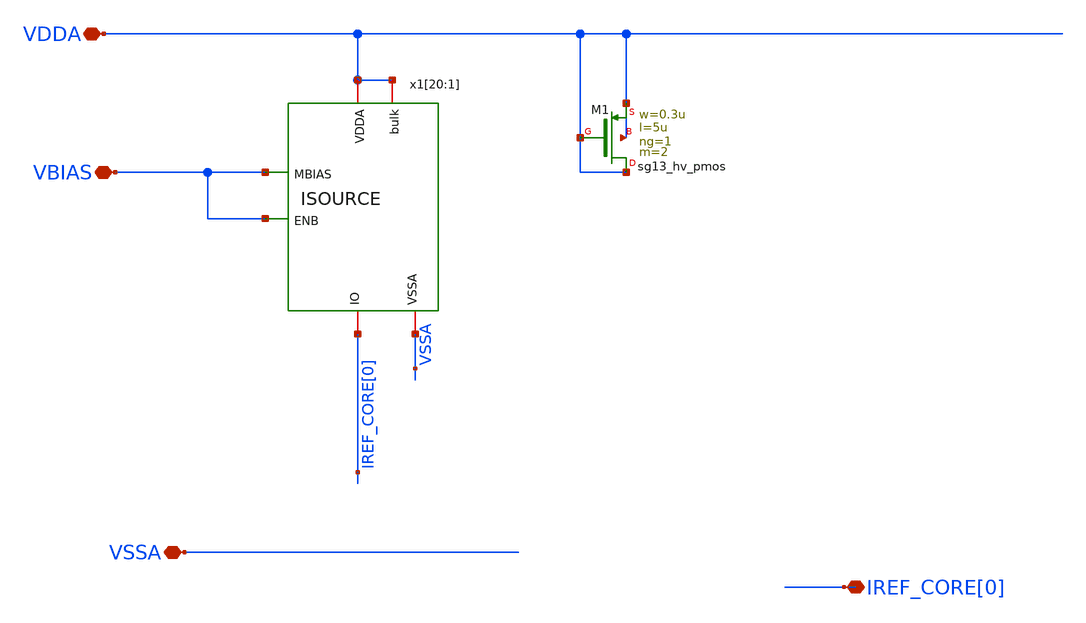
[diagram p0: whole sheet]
** sch_path: DecadeDividerAux.sch
**.subckt DecadeDividerAux VSSA VDDA VBIAS IREF_CORE[0]
*.iopin VSSA
*.iopin VDDA
*.iopin VBIAS
*.iopin IREF_CORE[0]
x1[20] VDDA VBIAS VDDA VBIAS VSSA IREF_CORE[0] ISOURCE
x1[19] VDDA VBIAS VDDA VBIAS VSSA IREF_CORE[0] ISOURCE
x1[18] VDDA VBIAS VDDA VBIAS VSSA IREF_CORE[0] ISOURCE
x1[17] VDDA VBIAS VDDA VBIAS VSSA IREF_CORE[0] ISOURCE
x1[16] VDDA VBIAS VDDA VBIAS VSSA IREF_CORE[0] ISOURCE
x1[15] VDDA VBIAS VDDA VBIAS VSSA IREF_CORE[0] ISOURCE
x1[14] VDDA VBIAS VDDA VBIAS VSSA IREF_CORE[0] ISOURCE
x1[13] VDDA VBIAS VDDA VBIAS VSSA IREF_CORE[0] ISOURCE
x1[12] VDDA VBIAS VDDA VBIAS VSSA IREF_CORE[0] ISOURCE
x1[11] VDDA VBIAS VDDA VBIAS VSSA IREF_CORE[0] ISOURCE
x1[10] VDDA VBIAS VDDA VBIAS VSSA IREF_CORE[0] ISOURCE
x1[9] VDDA VBIAS VDDA VBIAS VSSA IREF_CORE[0] ISOURCE
x1[8] VDDA VBIAS VDDA VBIAS VSSA IREF_CORE[0] ISOURCE
x1[7] VDDA VBIAS VDDA VBIAS VSSA IREF_CORE[0] ISOURCE
x1[6] VDDA VBIAS VDDA VBIAS VSSA IREF_CORE[0] ISOURCE
x1[5] VDDA VBIAS VDDA VBIAS VSSA IREF_CORE[0] ISOURCE
x1[4] VDDA VBIAS VDDA VBIAS VSSA IREF_CORE[0] ISOURCE
x1[3] VDDA VBIAS VDDA VBIAS VSSA IREF_CORE[0] ISOURCE
x1[2] VDDA VBIAS VDDA VBIAS VSSA IREF_CORE[0] ISOURCE
x1[1] VDDA VBIAS VDDA VBIAS VSSA IREF_CORE[0] ISOURCE
XM1 VDDA VDDA VDDA VDDA sg13_hv_pmos w=0.3u l=5u ng=1 m=2 mm_ok=1
**.ends
.end
